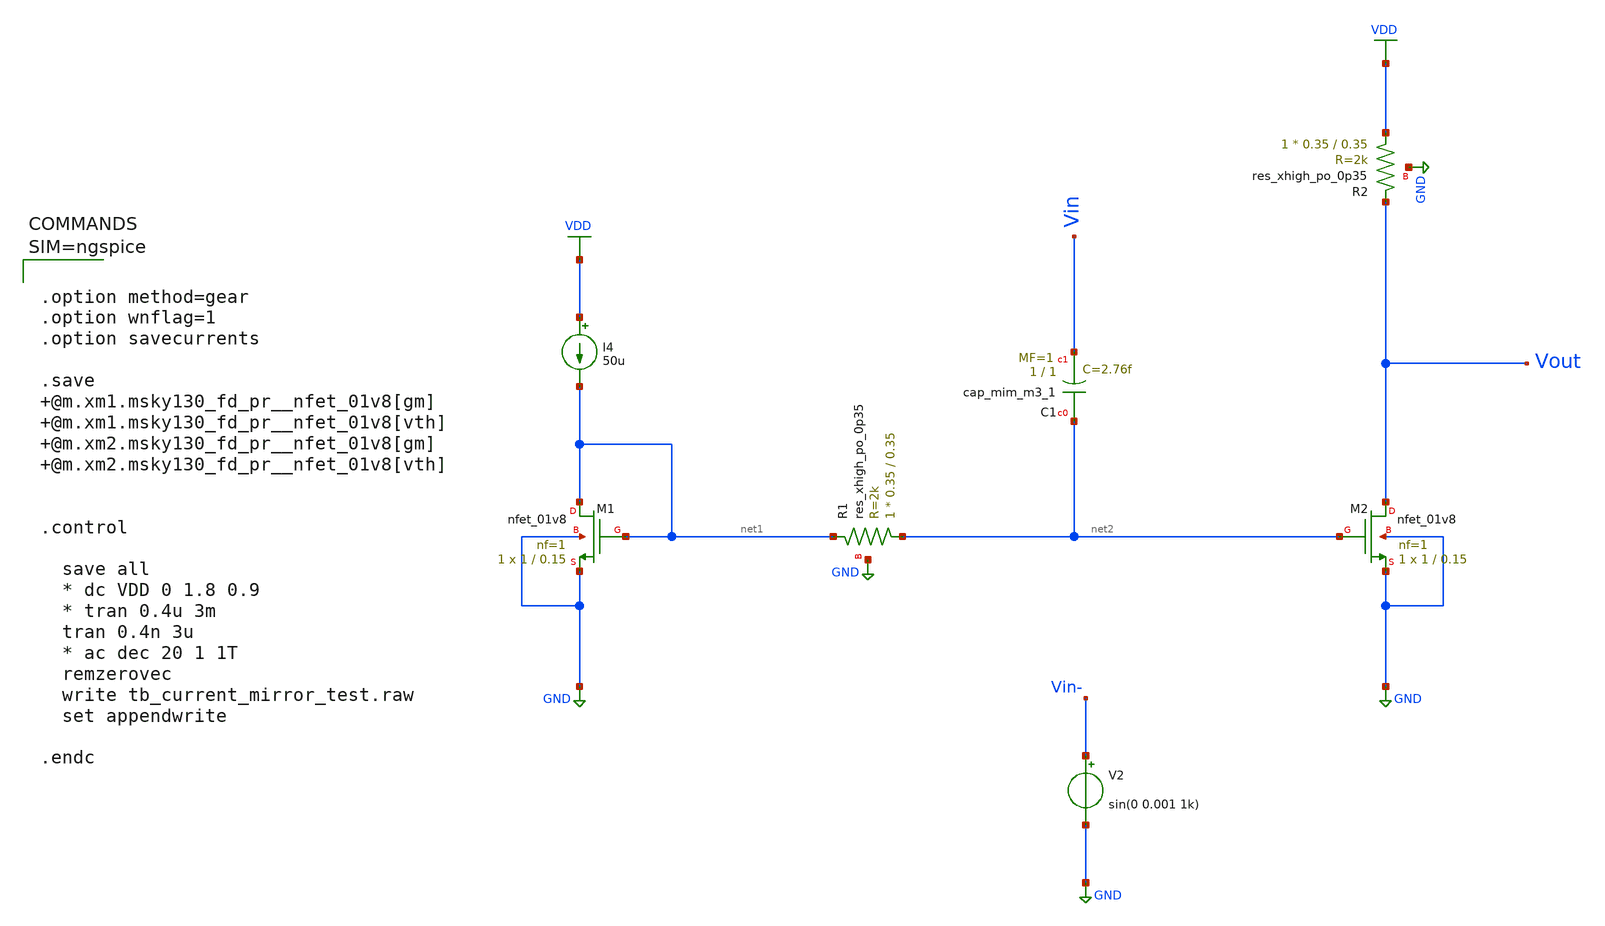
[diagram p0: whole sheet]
** sch_path: projects/opamp/xschem_ngspice/current_mirror_test.sch
**.subckt current_mirror_test
I4 VDD net1 50u
XM1 net1 net1 GND GND sky130_fd_pr__nfet_01v8 L=0.15 W=1 nf=1 ad='int((nf+1)/2) * W/nf * 0.29' as='int((nf+2)/2) * W/nf * 0.29'
+ pd='2*int((nf+1)/2) * (W/nf + 0.29)' ps='2*int((nf+2)/2) * (W/nf + 0.29)' nrd='0.29 / W' nrs='0.29 / W'
+ sa=0 sb=0 sd=0 mult=1 m=1
XR1 net2 net1 GND sky130_fd_pr__res_xhigh_po_0p35 L=0.35 mult=1 m=1
XM2 Vout net2 GND GND sky130_fd_pr__nfet_01v8 L=0.15 W=1 nf=1 ad='int((nf+1)/2) * W/nf * 0.29' as='int((nf+2)/2) * W/nf * 0.29'
+ pd='2*int((nf+1)/2) * (W/nf + 0.29)' ps='2*int((nf+2)/2) * (W/nf + 0.29)' nrd='0.29 / W' nrs='0.29 / W'
+ sa=0 sb=0 sd=0 mult=1 m=1
XR2 VDD Vout GND sky130_fd_pr__res_xhigh_po_0p35 L=0.35 mult=1 m=1
XC1 net2 Vin sky130_fd_pr__cap_mim_m3_1 W=1 L=1 MF=1 m=1
V2 Vin- GND sin(0 0.001 1k)
**** begin user architecture code



.option method=gear
.option wnflag=1
.option savecurrents

.save @m.xm1.msky130_fd_pr__nfet_01v8[gm] @m.xm1.msky130_fd_pr__nfet_01v8[vth] @m.xm2.msky130_fd_pr__nfet_01v8[gm] @m.xm2.msky130_fd_pr__nfet_01v8[vth]


.control

  save all
  * dc VDD 0 1.8 0.9
  * tran 0.4u 3m
  tran 0.4n 3u
  * ac dec 20 1 1T
  remzerovec
  write tb_current_mirror_test.raw
  set appendwrite

.endc




**** end user architecture code
**.ends
.GLOBAL VDD
.GLOBAL GND
.end
